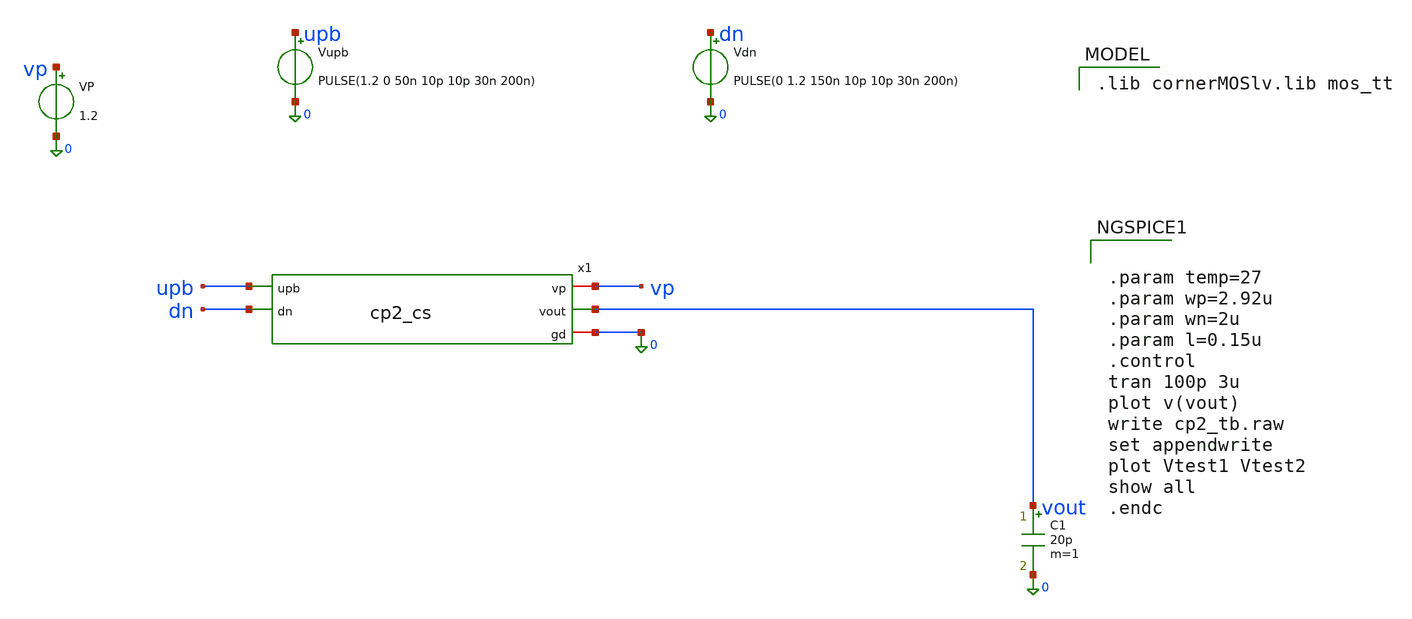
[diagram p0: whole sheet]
** sch_path: PLL0663-main/schematic/xschem/charge_pump/old_sch/cp_v2_tb.sch
**.subckt cp_v2_tb
C1 vout 0 20p m=1
VP vp 0 1.2
Vupb upb 0 PULSE(1.2 0 50n 10p 10p 30n 200n)
Vdn dn 0 PULSE(0 1.2 150n 10p 10p 30n 200n)
x1 vp upb vout dn 0 cp2_cs
**** begin user architecture code
 .lib cornerMOSlv.lib mos_tt



.param temp=27
.param wp=2.92u
.param wn=2u
.param l=0.15u
.control
tran 100p 3u
plot v(vout)
write cp2_tb.raw
set appendwrite
plot Vtest1 Vtest2
show all
.endc


**** end user architecture code
**.ends

* expanding   symbol:  /foss/designs/CHIP-PLL/charge_pump/cp2_cs.sym # of pins=5
** sym_path: charge_pump/cp2_cs.sym
** sch_path: charge_pump/cp2_cs.sch
.subckt cp2_cs vp upb vout dn gd
*.iopin vp
*.ipin upb
*.opin vout
*.ipin dn
*.iopin gd
XM3 net1 net1 vp vp sg13_lv_pmos w=2u l=0.15u ng=1 m=1 mm_ok=1
XM1 net8 net1 vp vp sg13_lv_pmos w=2u l=0.15u ng=1 m=1 mm_ok=1
XM6 vout upb net9 vp sg13_lv_pmos w=2u l=0.15u ng=1 m=1 mm_ok=1
XM9 vout dn net6 gd sg13_lv_nmos w=3u l=0.15u ng=1 m=1 mm_ok=1
XM10 net7 net2 gd gd sg13_lv_nmos w=3u l=0.15u ng=1 m=1 mm_ok=1
XM14 net2 net2 gd gd sg13_lv_nmos w=3u l=0.15u ng=1 m=1 mm_ok=1
XM13 iref iref vp vp sg13_lv_pmos w=2.2u l=0.15u ng=1 m=1 mm_ok=1
XM15 net3 iref vp vp sg13_lv_pmos w=1.8u l=0.15u ng=1 m=1 mm_ok=1
XM16 iref net3 net4 gd sg13_lv_nmos w=2.6u l=0.15u ng=1 m=1 mm_ok=1
XM17 net3 net3 gd gd sg13_lv_nmos w=2.2u l=0.15u ng=1 m=1 mm_ok=1
R1 net4 gd 500 m=1
XM20 net5 iref vp vp sg13_lv_pmos w=2u l=0.15u ng=1 m=1 mm_ok=1
XM21 iref_p net5 gd gd sg13_lv_nmos w=2u l=0.15u ng=1 m=1 mm_ok=1
XM22 net5 net5 gd gd sg13_lv_nmos w=2u l=0.15u ng=1 m=1 mm_ok=1
XM19 iref2 iref vp vp sg13_lv_pmos w=3u l=0.15u ng=1 m=1 mm_ok=1
Viup net8 net9 0
Vidn net6 net7 0
Viup1 net1 iref_p 0
Vidn1 iref2 net2 0
.ends

.end
